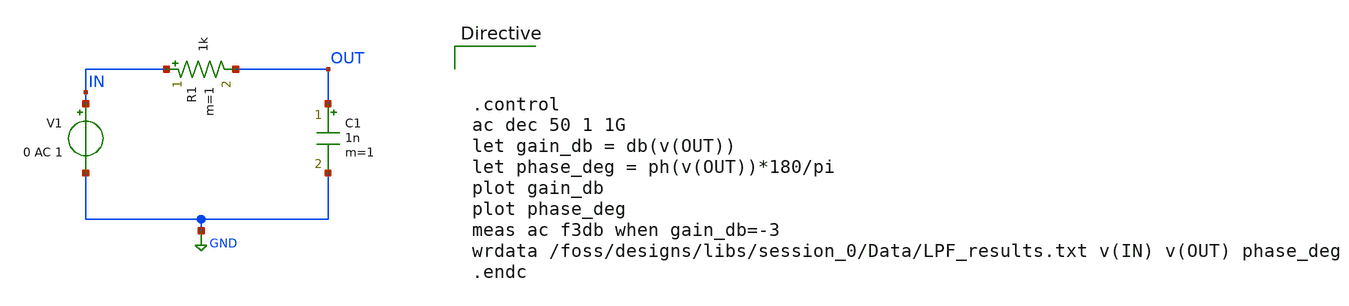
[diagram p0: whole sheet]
** sch_path: designs/libs/session_0/LPF.sch
**.subckt LPF
R1 IN OUT 1k m=1
C1 OUT GND 1n m=1
V1 IN GND 0 AC 1
**** begin user architecture code



.control
ac dec 50 1 1G
let gain_db = db(v(OUT))
let phase_deg = ph(v(OUT))*180/pi
plot gain_db
plot phase_deg
meas ac f3db when gain_db=-3
wrdata /foss/designs/libs/session_0/Data/LPF_results.txt v(IN) v(OUT) phase_deg
.endc



**** end user architecture code
**.ends
.GLOBAL GND
.end
